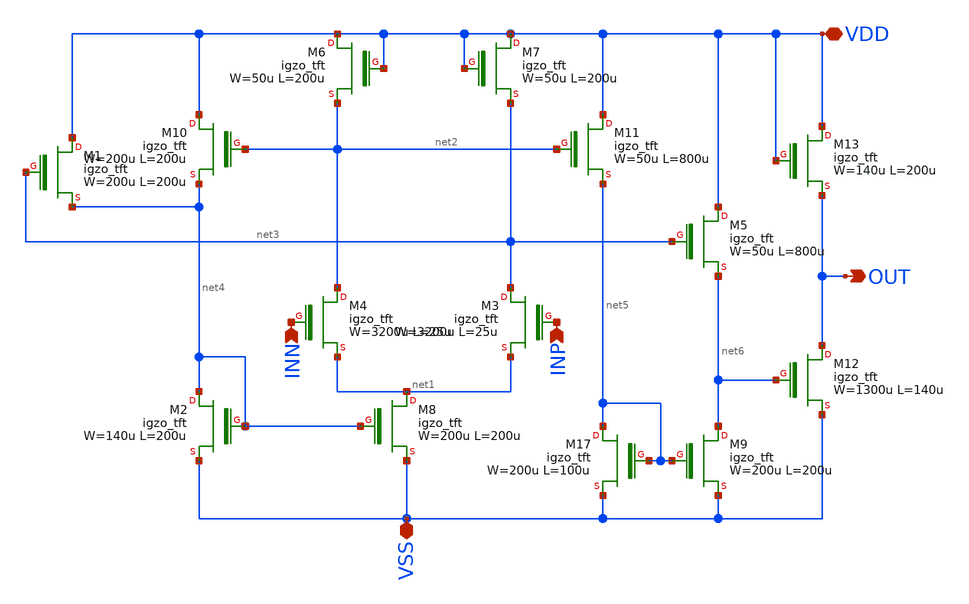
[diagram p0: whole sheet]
** sch_path: OPAM/OPAM2.sch
**.subckt OPAM2 VDD INN VSS OUT INP
*.iopin VDD
*.ipin INN
*.iopin VSS
*.opin OUT
*.ipin INP
XM4 net2 INN net1 igzo_tft W=3200u L=25u ov=5u nf=1 m=1
XM3 net3 INP net1 igzo_tft W=3200u L=25u ov=5u nf=1 m=1
XM6 VDD VDD net2 igzo_tft W=50u L=200u ov=5u nf=1 m=1
XM7 VDD VDD net3 igzo_tft W=50u L=200u ov=5u nf=1 m=1
XM8 net1 net4 VSS igzo_tft W=200u L=200u ov=5u nf=1 m=1
XM10 VDD net2 net4 igzo_tft W=200u L=200u ov=5u nf=1 m=1
XM17 net5 net5 VSS igzo_tft W=200u L=100u ov=5u nf=1 m=1
XM1 VDD net3 net4 igzo_tft W=200u L=200u ov=5u nf=1 m=1
XM2 net4 net4 VSS igzo_tft W=140u L=200u ov=5u nf=1 m=1
XM9 net6 net5 VSS igzo_tft W=200u L=200u ov=5u nf=1 m=1
XM11 VDD net2 net5 igzo_tft W=50u L=800u ov=5u nf=1 m=1
XM5 VDD net3 net6 igzo_tft W=50u L=800u ov=5u nf=1 m=1
XM12 OUT net6 VSS igzo_tft W=1300u L=140u ov=5u nf=1 m=1
XM13 VDD VDD OUT igzo_tft W=140u L=200u ov=5u nf=1 m=1
**.ends
.end
